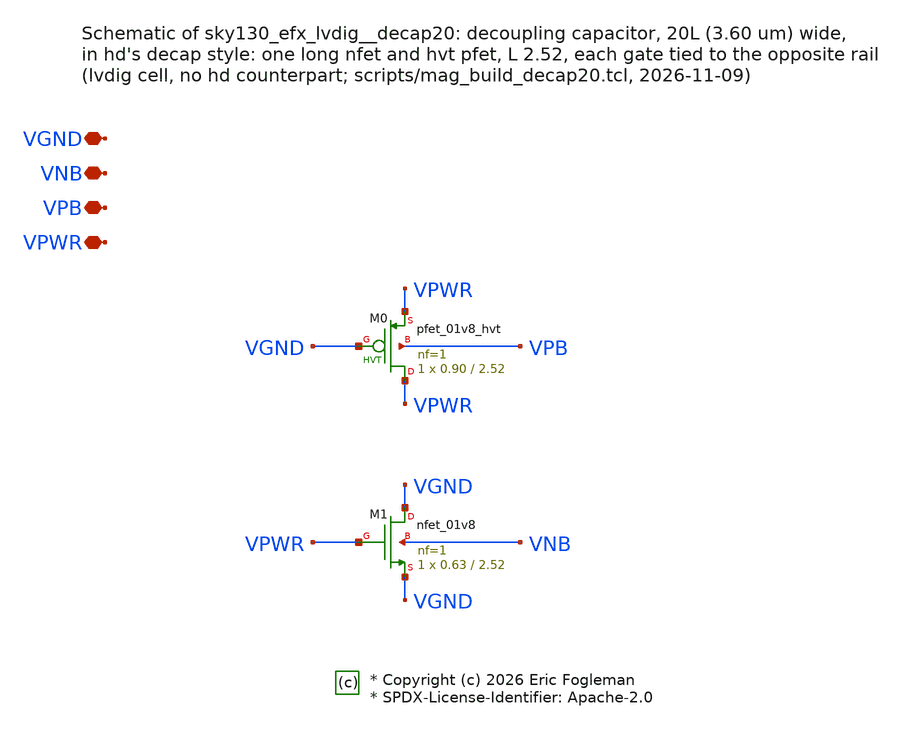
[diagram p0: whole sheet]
** sch_path: xschem/sky130_efx_lvdig__decap20.sch

* Copyright (c) 2026 Eric Fogleman
* SPDX-License-Identifier: Apache-2.0

**.subckt sky130_efx_lvdig__decap20 VGND VNB VPB VPWR
*.iopin VGND
*.iopin VNB
*.iopin VPB
*.iopin VPWR
XM0 VPWR VGND VPWR VPB sky130_fd_pr__pfet_01v8_hvt L=2.52 W=0.90 nf=1 ad='int((1 + 1)/2) * 0.90 / 1 * 0.29'
+ as='int((1 + 2)/2) * 0.90 / 1 * 0.29' pd='2*int((1 + 1)/2) * (0.90 / 1 + 0.29)' ps='2*int((1 + 2)/2) * (0.90 / 1 + 0.29)'
+ nrd='0.29 / 0.90 ' nrs='0.29 / 0.90 ' sa=0 sb=0 sd=0 mult=1 m=1
XM1 VGND VPWR VGND VNB sky130_fd_pr__nfet_01v8 L=2.52 W=0.63 nf=1 ad='int((1 + 1)/2) * 0.63 / 1 * 0.29'
+ as='int((1 + 2)/2) * 0.63 / 1 * 0.29' pd='2*int((1 + 1)/2) * (0.63 / 1 + 0.29)' ps='2*int((1 + 2)/2) * (0.63 / 1 + 0.29)'
+ nrd='0.29 / 0.63 ' nrs='0.29 / 0.63 ' sa=0 sb=0 sd=0 mult=1 m=1
**.ends
.end
